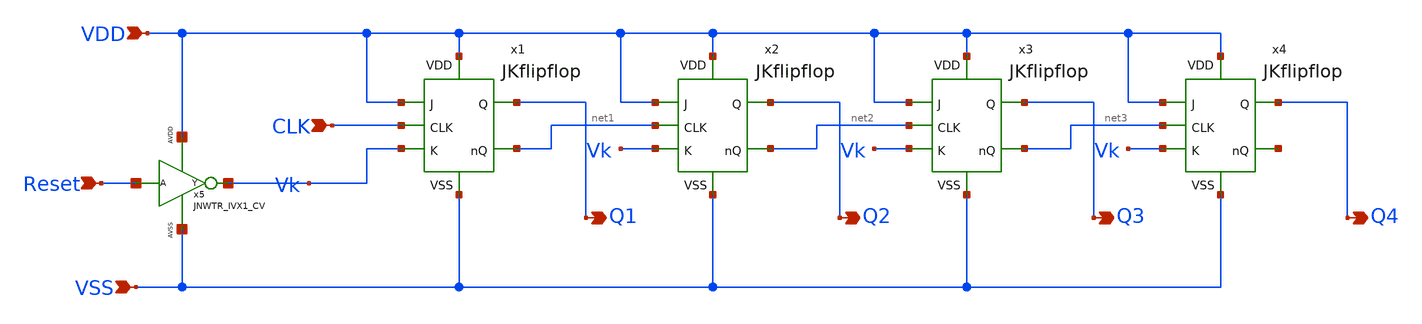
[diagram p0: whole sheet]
** sch_path: design/JNW_GR05_SKY130A/asynCounter.sch
**.subckt asynCounter VDD Q1 VSS CLK Q2 Q3 Q4 Reset
*.ipin VDD
*.opin Q1
*.ipin VSS
*.ipin CLK
*.opin Q2
*.opin Q3
*.opin Q4
*.ipin Reset
x1 VDD VDD Q1 CLK net1 Vk VSS JKflipflop
x2 VDD VDD Q2 net1 net2 Vk VSS JKflipflop
x3 VDD VDD Q3 net2 net3 Vk VSS JKflipflop
x4 VDD VDD Q4 net3 net4 Vk VSS JKflipflop
x5 Reset Vk VDD VSS JNWTR_IVX1_CV
**.ends
.end
